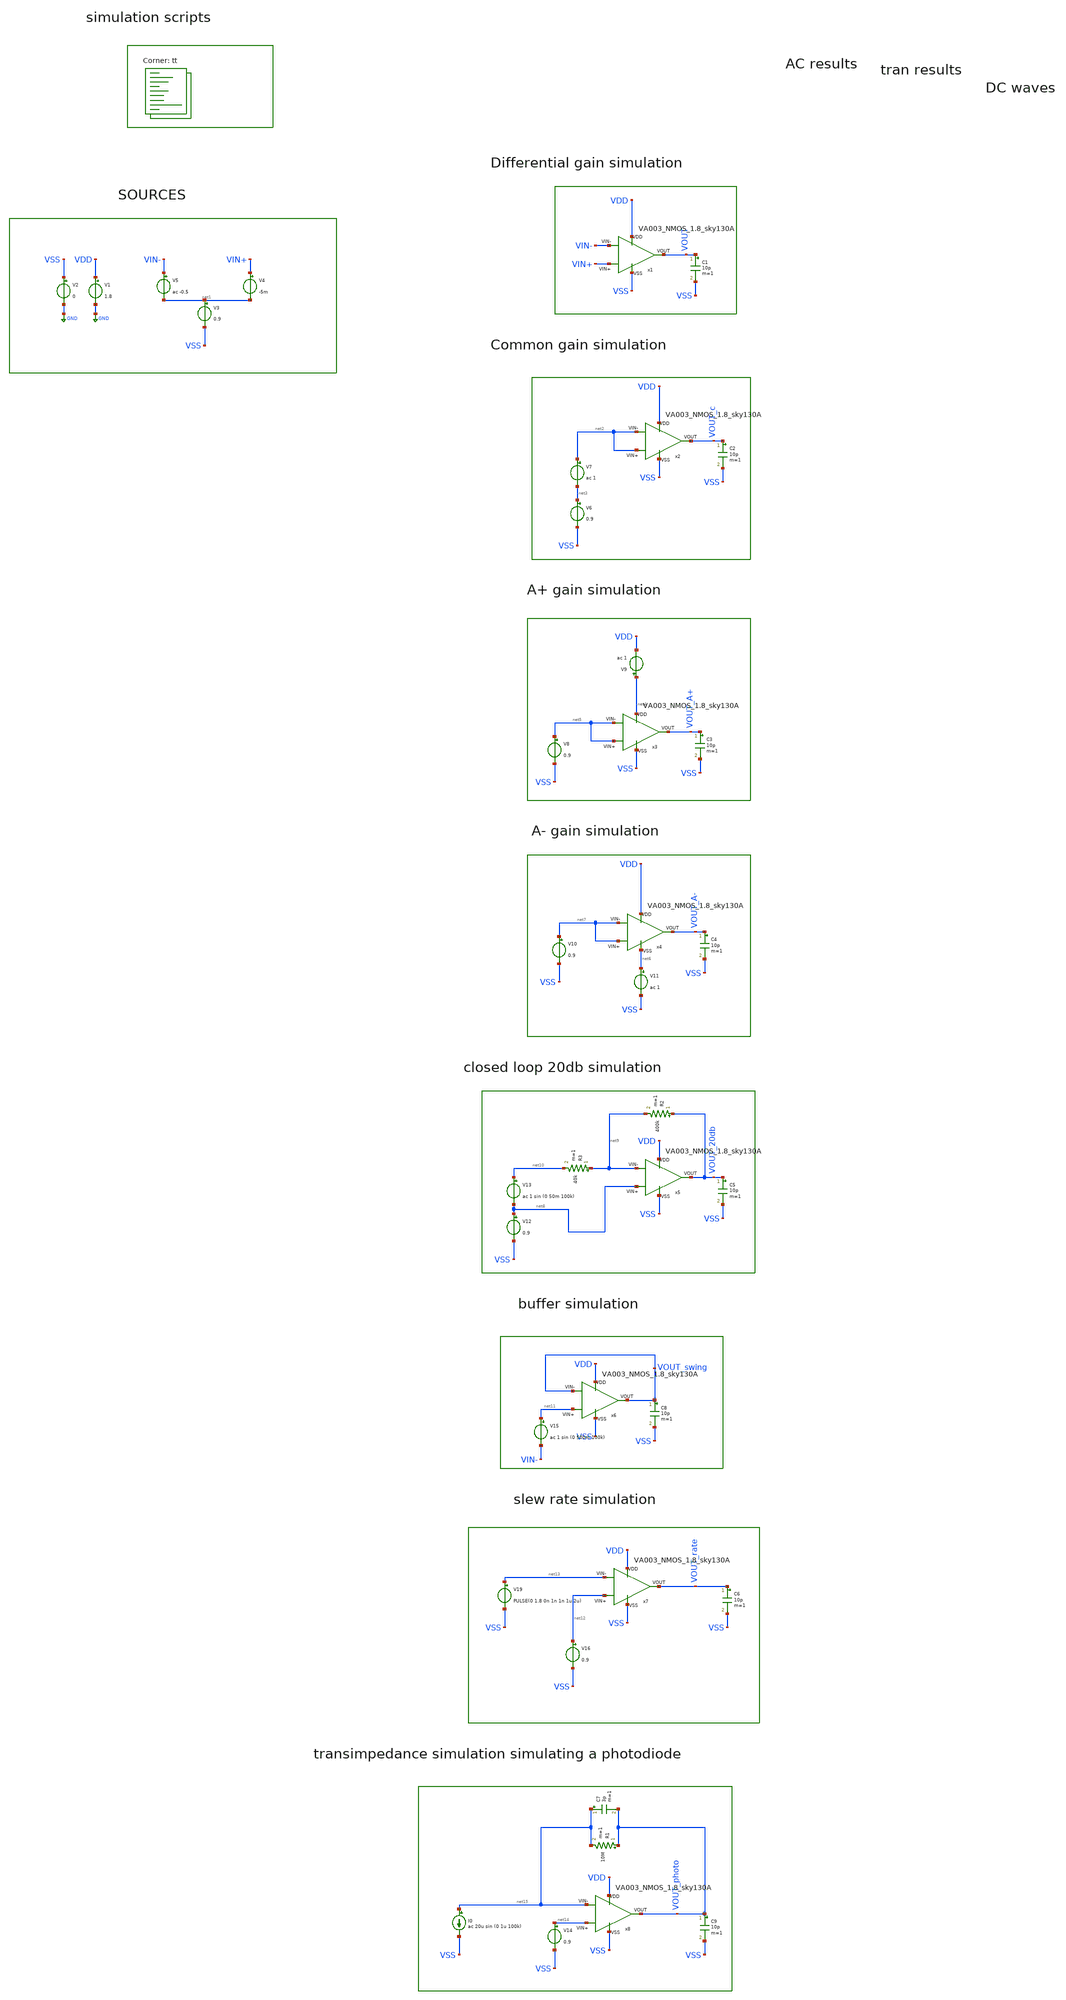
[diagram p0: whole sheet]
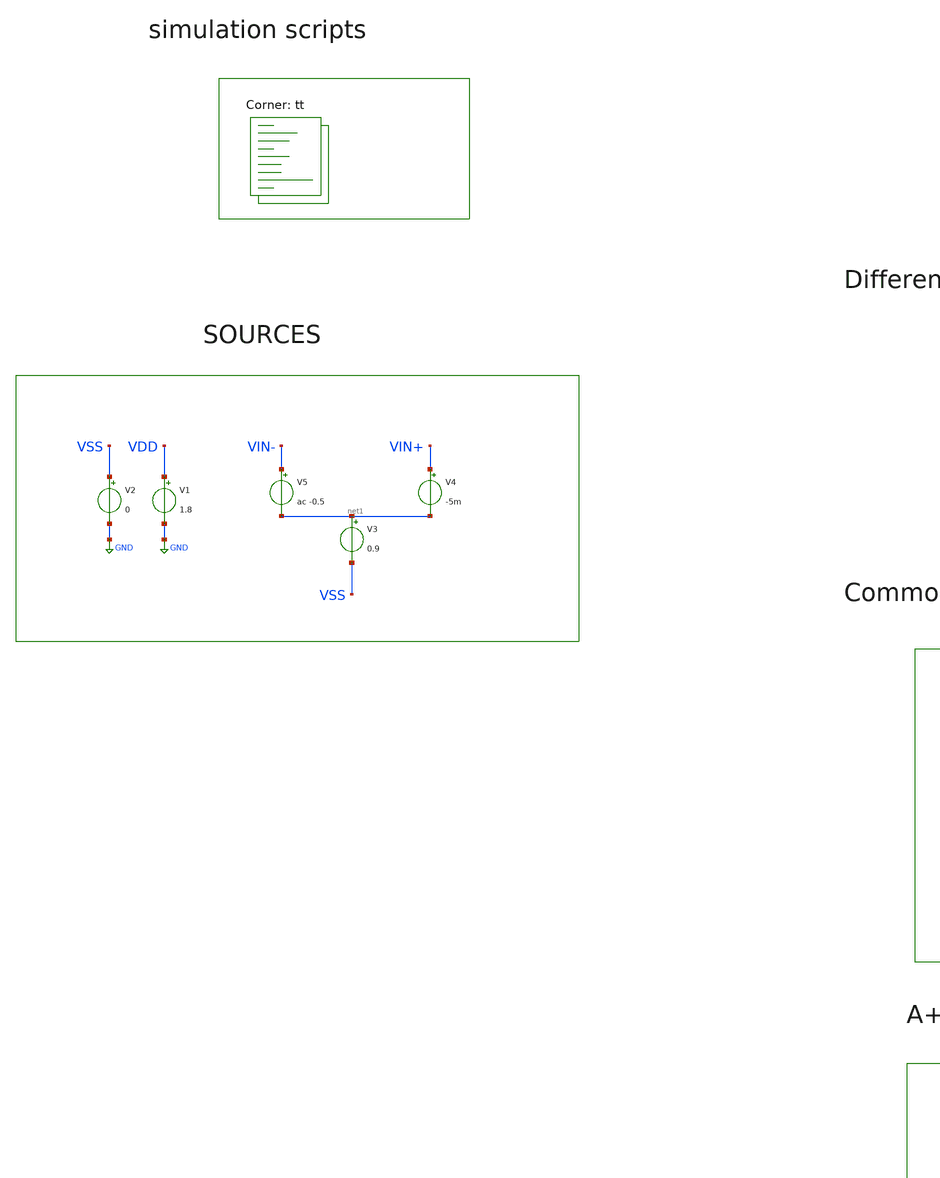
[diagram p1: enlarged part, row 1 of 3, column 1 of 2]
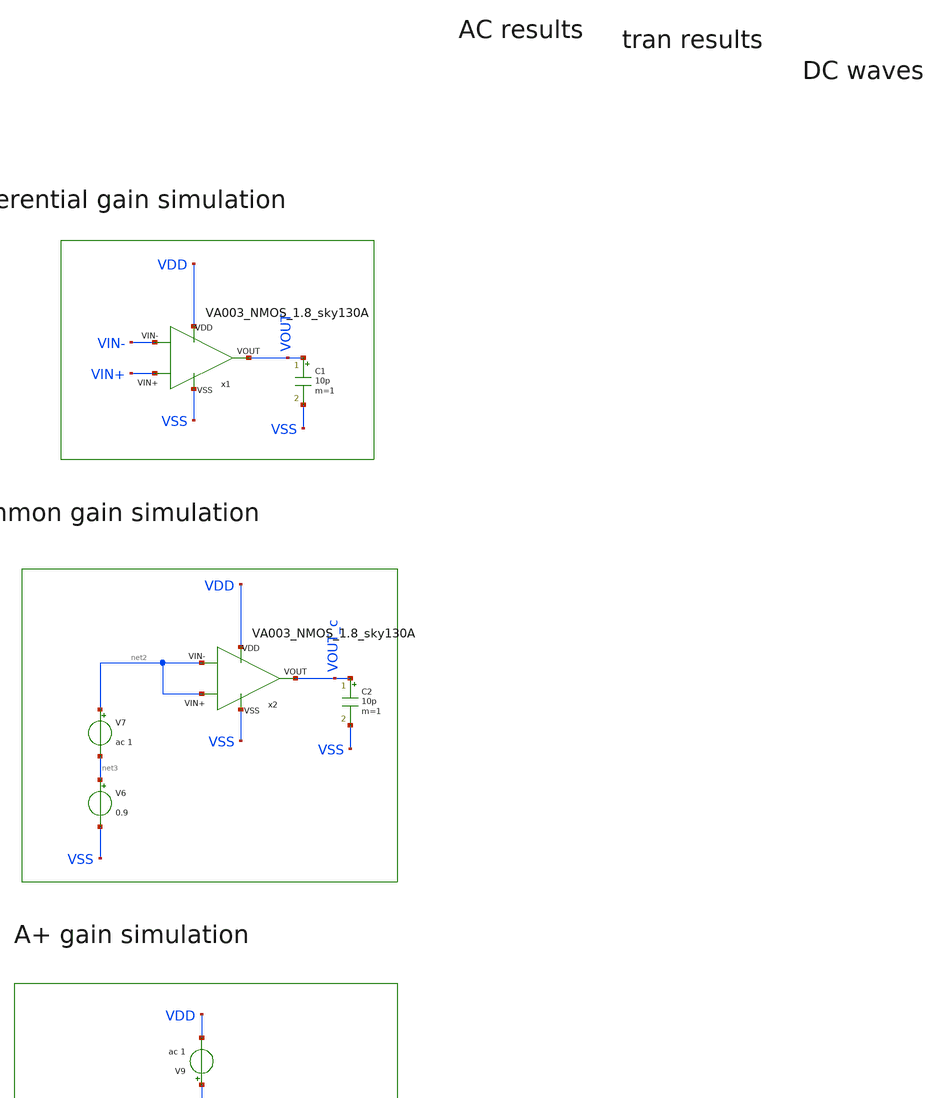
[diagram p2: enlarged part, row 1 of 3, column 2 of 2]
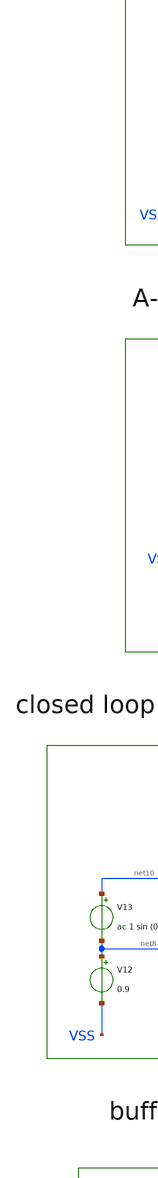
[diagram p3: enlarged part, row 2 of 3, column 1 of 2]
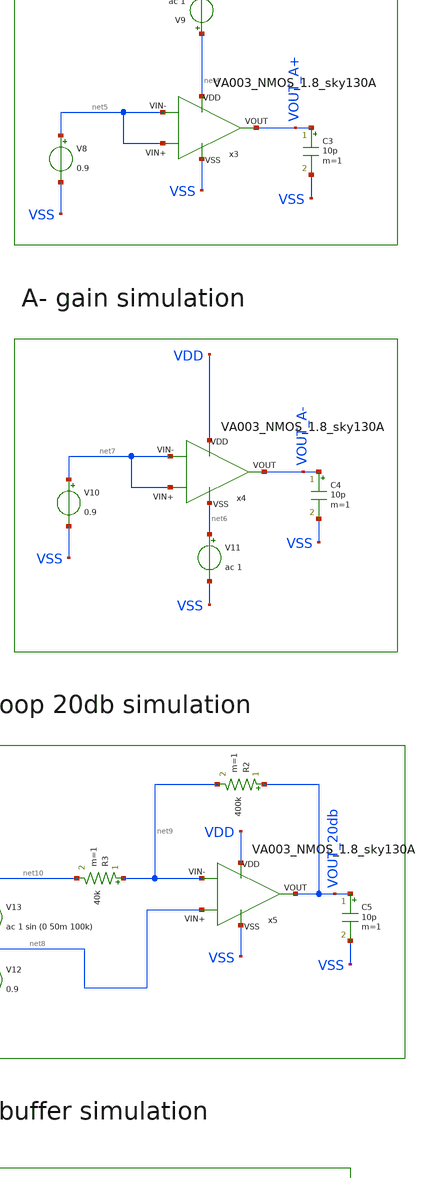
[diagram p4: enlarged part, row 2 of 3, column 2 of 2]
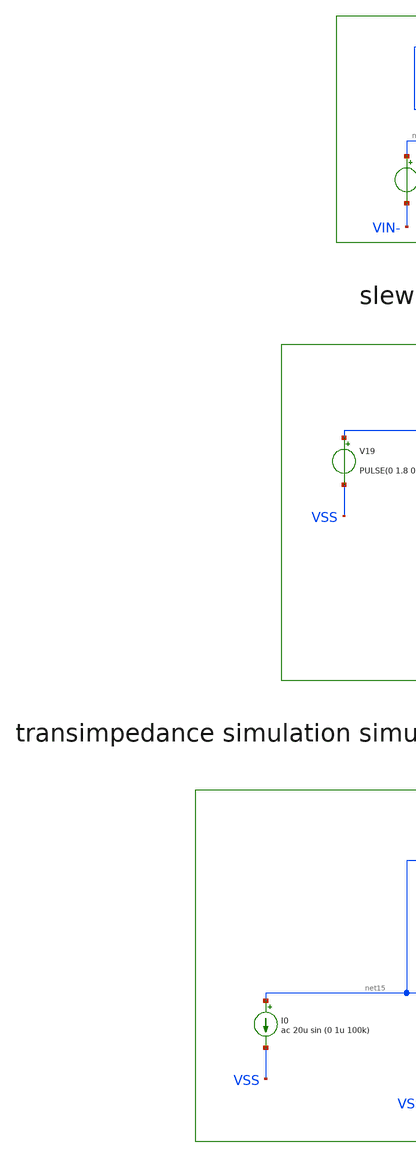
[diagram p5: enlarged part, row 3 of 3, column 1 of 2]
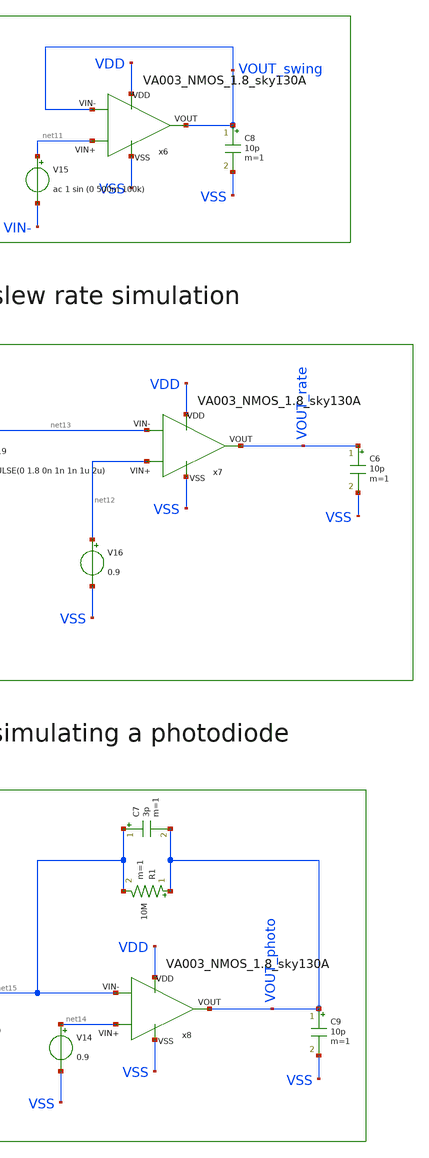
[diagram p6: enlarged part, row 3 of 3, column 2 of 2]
** sch_path: my_ip/sky130A/single_ended_OTAS_testbenches/tb.sch
**.subckt tb
V1 VDD GND 1.8
V2 VSS GND 0
V3 net1 VSS 0.9
V4 VIN+ net1 -5m
V5 VIN- net1 ac -0.5
C1 VOUT VSS 10p m=1
C2 VOUT_c VSS 10p m=1
V6 net3 VSS 0.9
V7 net2 net3 ac 1
C3 VOUT_A+ VSS 10p m=1
V8 net5 VSS 0.9
V9 net4 VDD ac 1
C4 VOUT_A- VSS 10p m=1
V10 net7 VSS 0.9
V11 net6 VSS ac 1
R2 VOUT_20db net9 400k m=1
R3 net9 net10 40k m=1
V12 net8 VSS 0.9
V13 net10 net8 ac 1 sin (0 50m 100k)
C5 VOUT_20db VSS 10p m=1
V15 net11 VIN- ac 1 sin (0 500m 100k)
V16 net12 VSS 0.9
C6 VOUT_rate VSS 10p m=1
V19 net13 VSS PULSE(0 1.8 0n 1n 1n 1u 2u)
C7 net15 VOUT_photo 3p m=1
V14 net14 VSS 0.9
R1 VOUT_photo net15 10M m=1
I0 net15 VSS ac 20u sin (0 1u 100k)
C8 VOUT_swing VSS 10p m=1
C9 VOUT_photo VSS 10p m=1
x1 VDD VSS VIN- VIN+ VOUT VA003_NMOS_1.8_sky130A
x2 VDD VSS net2 net2 VOUT_c VA003_NMOS_1.8_sky130A
x3 net4 VSS net5 net5 VOUT_A+ VA003_NMOS_1.8_sky130A
x4 VDD net6 net7 net7 VOUT_A- VA003_NMOS_1.8_sky130A
x5 VDD VSS net9 net8 VOUT_20db VA003_NMOS_1.8_sky130A
x6 VDD VSS VOUT_swing net11 VOUT_swing VA003_NMOS_1.8_sky130A
x7 VDD VSS net13 net12 VOUT_rate VA003_NMOS_1.8_sky130A
x8 VDD VSS net15 net14 VOUT_photo VA003_NMOS_1.8_sky130A
**** begin user architecture code
.lib $::SKYWATER_MODELS/sky130.lib.spice tt

**************************************************************
**************************************************************
**************************************************************
**************************************************************
**************************************************************
*LIBs*********************************************************
**************************************************************
**************************************************************
**************************************************************
**************************************************************
**************************************************************
*.lib $::SKYWATER_MODELS/sky130.lib.spice tt
* chose the corners in the corner file
* tt_mm for mismatch
* ss ff sf fs standart corners
* ll hh lh hl capacitor and resistors corners
* mc for total process variation including corners
**************************************************************
**************************************************************
**************************************************************
**************************************************************
**************************************************************
*Corners/montecarlo options***********************************
**************************************************************
**************************************************************
**************************************************************
**************************************************************
**************************************************************
.TEMP 27
**************************************************************
**************************************************************
**************************************************************
**************************************************************
*SIMULATION and Plots*****************************************
**************************************************************
**************************************************************
**************************************************************
**************************************************************
.control
save all
save @m.x1.xm1.msky130_fd_pr__pfet_01v8_lvt[gm]
save @m.x1.xm1.msky130_fd_pr__pfet_01v8_lvt[vth]
save @m.x1.xm1.msky130_fd_pr__pfet_01v8_lvt[gds]
save @m.x1.xm1.msky130_fd_pr__pfet_01v8_lvt[gmbs]
save @m.x1.xm1.msky130_fd_pr__pfet_01v8_lvt[vds]
save @m.x1.xm1.msky130_fd_pr__pfet_01v8_lvt[vgs]


save @m.x1.xm2.msky130_fd_pr__pfet_01v8_lvt[gm]
save @m.x1.xm2.msky130_fd_pr__pfet_01v8_lvt[vth]
save @m.x1.xm2.msky130_fd_pr__pfet_01v8_lvt[gds]
save @m.x1.xm2.msky130_fd_pr__pfet_01v8_lvt[gmbs]
save @m.x1.xm2.msky130_fd_pr__pfet_01v8_lvt[vds]
save @m.x1.xm2.msky130_fd_pr__pfet_01v8_lvt[vgs]

save @m.x1.xm3.msky130_fd_pr__nfet_01v8[gm]
save @m.x1.xm3.msky130_fd_pr__nfet_01v8[vth]
save @m.x1.xm3.msky130_fd_pr__nfet_01v8[gds]
save @m.x1.xm3.msky130_fd_pr__nfet_01v8[gmbs]
save @m.x1.xm3.msky130_fd_pr__nfet_01v8[vds]
save @m.x1.xm3.msky130_fd_pr__nfet_01v8[vgs]

save @m.x1.xm4.msky130_fd_pr__nfet_01v8[gm]
save @m.x1.xm4.msky130_fd_pr__nfet_01v8[vth]
save @m.x1.xm4.msky130_fd_pr__nfet_01v8[gds]
save @m.x1.xm4.msky130_fd_pr__nfet_01v8[gmbs]
save @m.x1.xm4.msky130_fd_pr__nfet_01v8[vds]
save @m.x1.xm4.msky130_fd_pr__nfet_01v8[vgs]

save @m.x1.xm5.msky130_fd_pr__nfet_01v8[gm]
save @m.x1.xm5.msky130_fd_pr__nfet_01v8[vth]
save @m.x1.xm5.msky130_fd_pr__nfet_01v8[gds]
save @m.x1.xm5.msky130_fd_pr__nfet_01v8[gmbs]
save @m.x1.xm5.msky130_fd_pr__nfet_01v8[vds]
save @m.x1.xm5.msky130_fd_pr__nfet_01v8[vgs]

save @m.x1.xm6.msky130_fd_pr__nfet_01v8[gm]
save @m.x1.xm6.msky130_fd_pr__nfet_01v8[vth]
save @m.x1.xm6.msky130_fd_pr__nfet_01v8[gds]
save @m.x1.xm6.msky130_fd_pr__nfet_01v8[gmbs]
save @m.x1.xm6.msky130_fd_pr__nfet_01v8[vds]
save @m.x1.xm6.msky130_fd_pr__nfet_01v8[vgs]

save @m.x1.xm7.msky130_fd_pr__pfet_01v8_lvt[gm]
save @m.x1.xm7.msky130_fd_pr__pfet_01v8_lvt[vth]
save @m.x1.xm7.msky130_fd_pr__pfet_01v8_lvt[gds]
save @m.x1.xm7.msky130_fd_pr__pfet_01v8_lvt[gmbs]
save @m.x1.xm7.msky130_fd_pr__pfet_01v8_lvt[vds]
save @m.x1.xm7.msky130_fd_pr__pfet_01v8_lvt[vgs]

save @m.x1.xm8.msky130_fd_pr__pfet_01v8_lvt[gm]
save @m.x1.xm8.msky130_fd_pr__pfet_01v8_lvt[vth]
save @m.x1.xm8.msky130_fd_pr__pfet_01v8_lvt[gds]
save @m.x1.xm8.msky130_fd_pr__pfet_01v8_lvt[gmbs]
save @m.x1.xm8.msky130_fd_pr__pfet_01v8_lvt[vds]
save @m.x1.xm8.msky130_fd_pr__pfet_01v8_lvt[vgs]

save @m.x1.xm9.msky130_fd_pr__pfet_01v8_lvt[gm]
save @m.x1.xm9.msky130_fd_pr__pfet_01v8_lvt[vth]
save @m.x1.xm9.msky130_fd_pr__pfet_01v8_lvt[gds]
save @m.x1.xm9.msky130_fd_pr__pfet_01v8_lvt[gmbs]
save @m.x1.xm9.msky130_fd_pr__pfet_01v8_lvt[vds]
save @m.x1.xm9.msky130_fd_pr__pfet_01v8_lvt[vgs]


save @m.x1.xm10.msky130_fd_pr__nfet_01v8[gm]
save @m.x1.xm10.msky130_fd_pr__nfet_01v8[vth]
save @m.x1.xm10.msky130_fd_pr__nfet_01v8[gds]
save @m.x1.xm10.msky130_fd_pr__nfet_01v8[gmbs]
save @m.x1.xm10.msky130_fd_pr__nfet_01v8[vds]
save @m.x1.xm10.msky130_fd_pr__nfet_01v8[vgs]


save @m.x1.xm11.msky130_fd_pr__nfet_01v8[gm]
save @m.x1.xm11.msky130_fd_pr__nfet_01v8[vth]
save @m.x1.xm11.msky130_fd_pr__nfet_01v8[gds]
save @m.x1.xm11.msky130_fd_pr__nfet_01v8[gmbs]
save @m.x1.xm11.msky130_fd_pr__nfet_01v8[vds]
save @m.x1.xm11.msky130_fd_pr__nfet_01v8[vgs]

save @m.x1.xm12.msky130_fd_pr__pfet_01v8_lvt[gm]
save @m.x1.xm12.msky130_fd_pr__pfet_01v8_lvt[vth]
save @m.x1.xm12.msky130_fd_pr__pfet_01v8_lvt[gds]
save @m.x1.xm12.msky130_fd_pr__pfet_01v8_lvt[gmbs]
save @m.x1.xm12.msky130_fd_pr__pfet_01v8_lvt[vds]
save @m.x1.xm12.msky130_fd_pr__pfet_01v8_lvt[vgs]

save @m.x1.xm13.msky130_fd_pr__nfet_01v8[gm]
save @m.x1.xm13.msky130_fd_pr__nfet_01v8[vth]
save @m.x1.xm13.msky130_fd_pr__nfet_01v8[gds]
save @m.x1.xm13.msky130_fd_pr__nfet_01v8[gmbs]
save @m.x1.xm13.msky130_fd_pr__nfet_01v8[vds]
save @m.x1.xm13.msky130_fd_pr__nfet_01v8[vgs]

op
write tb.raw
set appendwrite

ac dec 10 1 50G
plot db(v(VOUT)) (180*ph(v(VOUT))/pi)
plot (db(v(VOUT))-db(v(VOUT_c)))
plot (db(v(VOUT))-db(v(VOUT_A+)))
plot (db(v(VOUT))-db(v(VOUT_A-)))
plot db(v(VOUT_amp))
set appendwrite
write tb.raw

tran 10ns 50u
set appendwrite
write tb.raw
noise v(VOUT,VSS) V4 dec 10 1 10G
set appendwrite
write tb.raw
plot inoise_spectrum

dc V3 0 1.8 0.001
set appendwrite
write tb.raw
.endc

**** end user architecture code
**.ends

* expanding   symbol:  single ended amplifiers/VA003_NMOS_1.8_sky130A.sym # of pins=5
** sym_path: my_ip/LIB/Sky130A/single ended amplifiers/VA003_NMOS_1.8_sky130A.sym
** sch_path: my_ip/LIB/Sky130A/single ended amplifiers/VA003_NMOS_1.8_sky130A.sch
.subckt VA003_NMOS_1.8_sky130A VDD VSS VIN- VIN+ VOUT
*.iopin VDD
*.iopin VSS
*.iopin VIN-
*.iopin VIN+
*.iopin VOUT
XR10 VSS net4 VSS sky130_fd_pr__res_xhigh_po_0p35 L=1.2 mult=2 m=2
XM4 net1 net2 net3 VSS sky130_fd_pr__nfet_01v8 L=3 W='2 * 2 ' nf=2 ad='int((2 + 1)/2) * 2 / 2 * 0.29'
+ as='int((2 + 2)/2) * 2 / 2 * 0.29' pd='2*int((2 + 1)/2) * (2 / 2 + 0.29)' ps='2*int((2 + 2)/2) * (2 / 2 + 0.29)'
+ nrd='0.29 / 2 ' nrs='0.29 / 2 ' sa=0 sb=0 sd=0 mult=4 m=4
XM3 net2 net2 V1 VSS sky130_fd_pr__nfet_01v8 L=3 W='2 * 2 ' nf=2 ad='int((2 + 1)/2) * 2 / 2 * 0.29' as='int((2 + 2)/2) * 2 / 2 * 0.29'
+ pd='2*int((2 + 1)/2) * (2 / 2 + 0.29)' ps='2*int((2 + 2)/2) * (2 / 2 + 0.29)' nrd='0.29 / 2 ' nrs='0.29 / 2 '
+ sa=0 sb=0 sd=0 mult=4 m=4
XM6 net3 V1 net4 VSS sky130_fd_pr__nfet_01v8 L=2 W='3 * 2 ' nf=2 ad='int((2 + 1)/2) * 3 / 2 * 0.29' as='int((2 + 2)/2) * 3 / 2 * 0.29'
+ pd='2*int((2 + 1)/2) * (3 / 2 + 0.29)' ps='2*int((2 + 2)/2) * (3 / 2 + 0.29)' nrd='0.29 / 3 ' nrs='0.29 / 3 '
+ sa=0 sb=0 sd=0 mult=8 m=8
XM5 V1 V1 VSS VSS sky130_fd_pr__nfet_01v8 L=2 W='3 * 2 ' nf=2 ad='int((2 + 1)/2) * 3 / 2 * 0.29' as='int((2 + 2)/2) * 3 / 2 * 0.29'
+ pd='2*int((2 + 1)/2) * (3 / 2 + 0.29)' ps='2*int((2 + 2)/2) * (3 / 2 + 0.29)' nrd='0.29 / 3 ' nrs='0.29 / 3 '
+ sa=0 sb=0 sd=0 mult=2 m=2
XM2 net2 net1 VDD VDD sky130_fd_pr__pfet_01v8_lvt L=3 W='4 * 2 ' nf=2 ad='int((2 + 1)/2) * 4 / 2 * 0.29'
+ as='int((2 + 2)/2) * 4 / 2 * 0.29' pd='2*int((2 + 1)/2) * (4 / 2 + 0.29)' ps='2*int((2 + 2)/2) * (4 / 2 + 0.29)'
+ nrd='0.29 / 4 ' nrs='0.29 / 4 ' sa=0 sb=0 sd=0 mult=2 m=2
XM1 net1 net1 VDD VDD sky130_fd_pr__pfet_01v8_lvt L=3 W='4 * 2 ' nf=2 ad='int((2 + 1)/2) * 4 / 2 * 0.29'
+ as='int((2 + 2)/2) * 4 / 2 * 0.29' pd='2*int((2 + 1)/2) * (4 / 2 + 0.29)' ps='2*int((2 + 2)/2) * (4 / 2 + 0.29)'
+ nrd='0.29 / 4 ' nrs='0.29 / 4 ' sa=0 sb=0 sd=0 mult=2 m=2
XM7 net5 V1 VSS VSS sky130_fd_pr__nfet_01v8 L=2 W='3 * 2 ' nf=2 ad='int((2 + 1)/2) * 3 / 2 * 0.29' as='int((2 + 2)/2) * 3 / 2 * 0.29'
+ pd='2*int((2 + 1)/2) * (3 / 2 + 0.29)' ps='2*int((2 + 2)/2) * (3 / 2 + 0.29)' nrd='0.29 / 3 ' nrs='0.29 / 3 '
+ sa=0 sb=0 sd=0 mult=24 m=24
XM34 net6 VIN+ net5 VSS sky130_fd_pr__nfet_01v8 L=1 W='6 * 4 ' nf=4 ad='int((4 + 1)/2) * 6 / 4 * 0.29'
+ as='int((4 + 2)/2) * 6 / 4 * 0.29' pd='2*int((4 + 1)/2) * (6 / 4 + 0.29)' ps='2*int((4 + 2)/2) * (6 / 4 + 0.29)'
+ nrd='0.29 / 6 ' nrs='0.29 / 6 ' sa=0 sb=0 sd=0 mult=4 m=4
XM8 net7 VIN- net5 VSS sky130_fd_pr__nfet_01v8 L=1 W='6 * 4 ' nf=4 ad='int((4 + 1)/2) * 6 / 4 * 0.29'
+ as='int((4 + 2)/2) * 6 / 4 * 0.29' pd='2*int((4 + 1)/2) * (6 / 4 + 0.29)' ps='2*int((4 + 2)/2) * (6 / 4 + 0.29)'
+ nrd='0.29 / 6 ' nrs='0.29 / 6 ' sa=0 sb=0 sd=0 mult=4 m=4
XM9 net6 net6 VDD VDD sky130_fd_pr__pfet_01v8_lvt L=1 W='3 * 2 ' nf=2 ad='int((2 + 1)/2) * 3 / 2 * 0.29'
+ as='int((2 + 2)/2) * 3 / 2 * 0.29' pd='2*int((2 + 1)/2) * (3 / 2 + 0.29)' ps='2*int((2 + 2)/2) * (3 / 2 + 0.29)'
+ nrd='0.29 / 3 ' nrs='0.29 / 3 ' sa=0 sb=0 sd=0 mult=2 m=2
XM10 net7 net6 VDD VDD sky130_fd_pr__pfet_01v8_lvt L=1 W='3 * 2 ' nf=2 ad='int((2 + 1)/2) * 3 / 2 * 0.29'
+ as='int((2 + 2)/2) * 3 / 2 * 0.29' pd='2*int((2 + 1)/2) * (3 / 2 + 0.29)' ps='2*int((2 + 2)/2) * (3 / 2 + 0.29)'
+ nrd='0.29 / 3 ' nrs='0.29 / 3 ' sa=0 sb=0 sd=0 mult=2 m=2
XM11 VB1 V1 VSS VSS sky130_fd_pr__nfet_01v8 L=2 W='3 * 2 ' nf=2 ad='int((2 + 1)/2) * 3 / 2 * 0.29' as='int((2 + 2)/2) * 3 / 2 * 0.29'
+ pd='2*int((2 + 1)/2) * (3 / 2 + 0.29)' ps='2*int((2 + 2)/2) * (3 / 2 + 0.29)' nrd='0.29 / 3 ' nrs='0.29 / 3 '
+ sa=0 sb=0 sd=0 mult=12 m=12
XR32 VB1 VB2 VSS sky130_fd_pr__res_xhigh_po_0p35 L=2 mult=2 m=2
XM13 VB2 VB1 net8 VDD sky130_fd_pr__pfet_01v8_lvt L=1 W='4 * 4 ' nf=4 ad='int((4 + 1)/2) * 4 / 4 * 0.29'
+ as='int((4 + 2)/2) * 4 / 4 * 0.29' pd='2*int((4 + 1)/2) * (4 / 4 + 0.29)' ps='2*int((4 + 2)/2) * (4 / 4 + 0.29)'
+ nrd='0.29 / 4 ' nrs='0.29 / 4 ' sa=0 sb=0 sd=0 mult=2 m=2
XM12 net8 VB2 VDD VDD sky130_fd_pr__pfet_01v8_lvt L=1 W='4 * 4 ' nf=4 ad='int((4 + 1)/2) * 4 / 4 * 0.29'
+ as='int((4 + 2)/2) * 4 / 4 * 0.29' pd='2*int((4 + 1)/2) * (4 / 4 + 0.29)' ps='2*int((4 + 2)/2) * (4 / 4 + 0.29)'
+ nrd='0.29 / 4 ' nrs='0.29 / 4 ' sa=0 sb=0 sd=0 mult=2 m=2
XM14 net9 VB2 VDD VDD sky130_fd_pr__pfet_01v8_lvt L=1 W='4 * 4 ' nf=4 ad='int((4 + 1)/2) * 4 / 4 * 0.29'
+ as='int((4 + 2)/2) * 4 / 4 * 0.29' pd='2*int((4 + 1)/2) * (4 / 4 + 0.29)' ps='2*int((4 + 2)/2) * (4 / 4 + 0.29)'
+ nrd='0.29 / 4 ' nrs='0.29 / 4 ' sa=0 sb=0 sd=0 mult=16 m=16
XM15 net10 VB1 net9 VDD sky130_fd_pr__pfet_01v8_lvt L=1 W='4 * 4 ' nf=4 ad='int((4 + 1)/2) * 4 / 4 * 0.29'
+ as='int((4 + 2)/2) * 4 / 4 * 0.29' pd='2*int((4 + 1)/2) * (4 / 4 + 0.29)' ps='2*int((4 + 2)/2) * (4 / 4 + 0.29)'
+ nrd='0.29 / 4 ' nrs='0.29 / 4 ' sa=0 sb=0 sd=0 mult=16 m=16
XM17 net11 net7 VOUT net10 sky130_fd_pr__pfet_01v8_lvt L=0.35 W='6 * 20 ' nf=20 ad='int((20 + 1)/2) * 6 / 20 * 0.29'
+ as='int((20 + 2)/2) * 6 / 20 * 0.29' pd='2*int((20 + 1)/2) * (6 / 20 + 0.29)' ps='2*int((20 + 2)/2) * (6 / 20 + 0.29)'
+ nrd='0.29 / 6 ' nrs='0.29 / 6 ' sa=0 sb=0 sd=0 mult=4 m=4
XM18 VSS net7 net11 net11 sky130_fd_pr__pfet_01v8_lvt L=0.35 W='6 * 20 ' nf=20 ad='int((20 + 1)/2) * 6 / 20 * 0.29'
+ as='int((20 + 2)/2) * 6 / 20 * 0.29' pd='2*int((20 + 1)/2) * (6 / 20 + 0.29)' ps='2*int((20 + 2)/2) * (6 / 20 + 0.29)'
+ nrd='0.29 / 6 ' nrs='0.29 / 6 ' sa=0 sb=0 sd=0 mult=4 m=4
XM16 VOUT VOUT net10 net10 sky130_fd_pr__pfet_01v8_lvt L=0.35 W='6 * 20 ' nf=20 ad='int((20 + 1)/2) * 6 / 20 * 0.29'
+ as='int((20 + 2)/2) * 6 / 20 * 0.29' pd='2*int((20 + 1)/2) * (6 / 20 + 0.29)' ps='2*int((20 + 2)/2) * (6 / 20 + 0.29)'
+ nrd='0.29 / 6 ' nrs='0.29 / 6 ' sa=0 sb=0 sd=0 mult=4 m=4
XR39 net12 net7 VSS sky130_fd_pr__res_xhigh_po_0p35 L=0.4 mult=2 m=2
XC1 VOUT net12 sky130_fd_pr__cap_mim_m3_2 W=9.6 L=9.6 MF=20 m=20
.ends

.GLOBAL GND
.end
